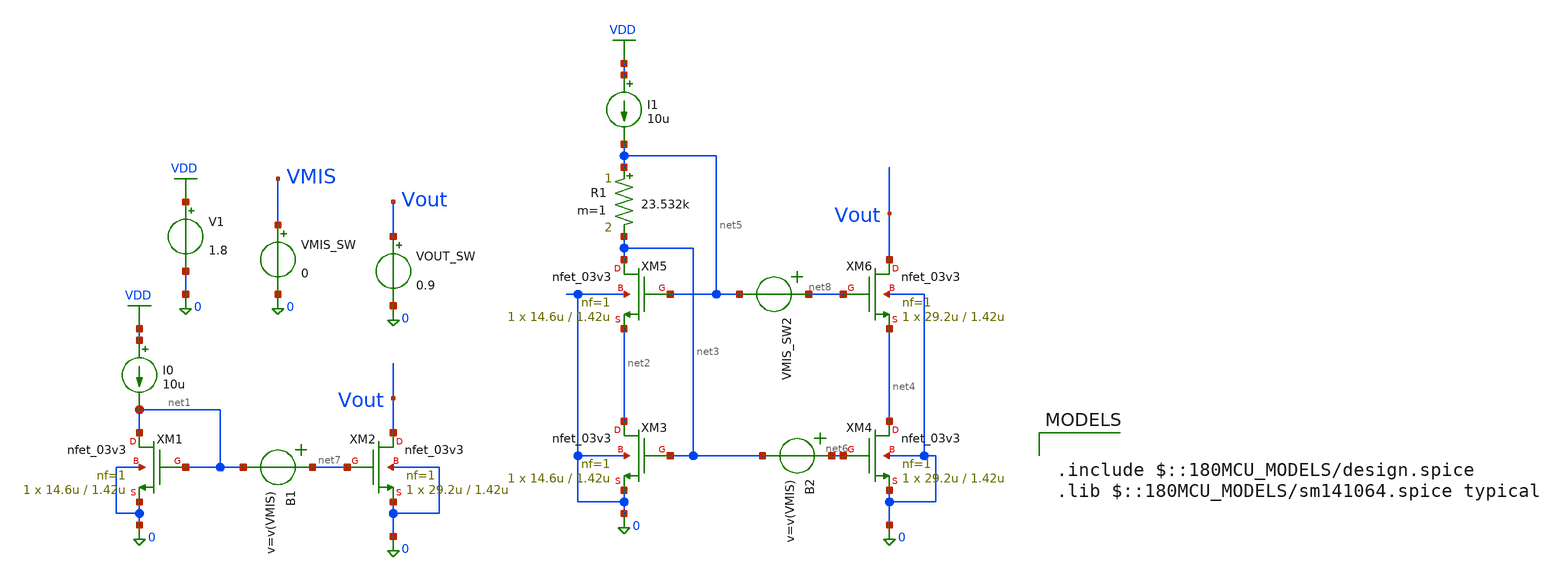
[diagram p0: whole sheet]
** sch_path: Lab_05/CMirror_mc.sch
**.subckt CMirror_mc
I0 VDD net1 10u
XM1 net1 net1 0 0 nfet_03v3 L=1.42u W=14.6u nf=1 ad='int((nf+1)/2) * W/nf * 0.18u' as='int((nf+2)/2) * W/nf * 0.18u'
+ pd='2*int((nf+1)/2) * (W/nf + 0.18u)' ps='2*int((nf+2)/2) * (W/nf + 0.18u)' nrd='0.18u / W' nrs='0.18u / W'
+ sa=0 sb=0 sd=0 m=1
XM2 Vout net7 0 0 nfet_03v3 L=1.42u W=29.2u nf=1 ad='int((nf+1)/2) * W/nf * 0.18u' as='int((nf+2)/2) * W/nf * 0.18u'
+ pd='2*int((nf+1)/2) * (W/nf + 0.18u)' ps='2*int((nf+2)/2) * (W/nf + 0.18u)' nrd='0.18u / W' nrs='0.18u / W'
+ sa=0 sb=0 sd=0 m=1
V1 VDD 0 1.8
XM3 net2 net3 0 0 nfet_03v3 L=1.42u W=14.6u nf=1 ad='int((nf+1)/2) * W/nf * 0.18u' as='int((nf+2)/2) * W/nf * 0.18u'
+ pd='2*int((nf+1)/2) * (W/nf + 0.18u)' ps='2*int((nf+2)/2) * (W/nf + 0.18u)' nrd='0.18u / W' nrs='0.18u / W'
+ sa=0 sb=0 sd=0 m=1
XM4 net4 net6 0 0 nfet_03v3 L=1.42u W=29.2u nf=1 ad='int((nf+1)/2) * W/nf * 0.18u' as='int((nf+2)/2) * W/nf * 0.18u'
+ pd='2*int((nf+1)/2) * (W/nf + 0.18u)' ps='2*int((nf+2)/2) * (W/nf + 0.18u)' nrd='0.18u / W' nrs='0.18u / W'
+ sa=0 sb=0 sd=0 m=1
XM5 net3 net5 net2 0 nfet_03v3 L=1.42u W=14.6u nf=1 ad='int((nf+1)/2) * W/nf * 0.18u' as='int((nf+2)/2) * W/nf * 0.18u'
+ pd='2*int((nf+1)/2) * (W/nf + 0.18u)' ps='2*int((nf+2)/2) * (W/nf + 0.18u)' nrd='0.18u / W' nrs='0.18u / W'
+ sa=0 sb=0 sd=0 m=1
I1 VDD net5 10u
R1 net5 net3 23.532k m=1
XM6 Vout net8 net4 0 nfet_03v3 L=1.42u W=29.2u nf=1 ad='int((nf+1)/2) * W/nf * 0.18u' as='int((nf+2)/2) * W/nf * 0.18u'
+ pd='2*int((nf+1)/2) * (W/nf + 0.18u)' ps='2*int((nf+2)/2) * (W/nf + 0.18u)' nrd='0.18u / W' nrs='0.18u / W'
+ sa=0 sb=0 sd=0 m=1
B1 net7 net1 v=v(VMIS)
VMIS_SW VMIS 0 0
VOUT_SW Vout 0 0.9
B2 net6 net3 v=v(VMIS)
VMIS_SW2 net8 net5
**** begin user architecture code


.control
shell rm MC_WS_CM.csv
shell rm MC_Simple_CM.csv
alterparam sw_stat_global = 1
alterparam sw_stat_mismatch = 1
reset
let mc_runs = 200
let run = 1
dowhile run <= mc_runs
op
print @m.xm2.m0[id] >> MC_Simple_CM.csv
print @m.xm4.m0[id] >> MC_WS_CM.csv
reset
let run = run + 1
end
.endc


.include $::180MCU_MODELS/design.spice
.lib $::180MCU_MODELS/sm141064.spice typical

**** end user architecture code
**.ends
.GLOBAL VDD
.end
